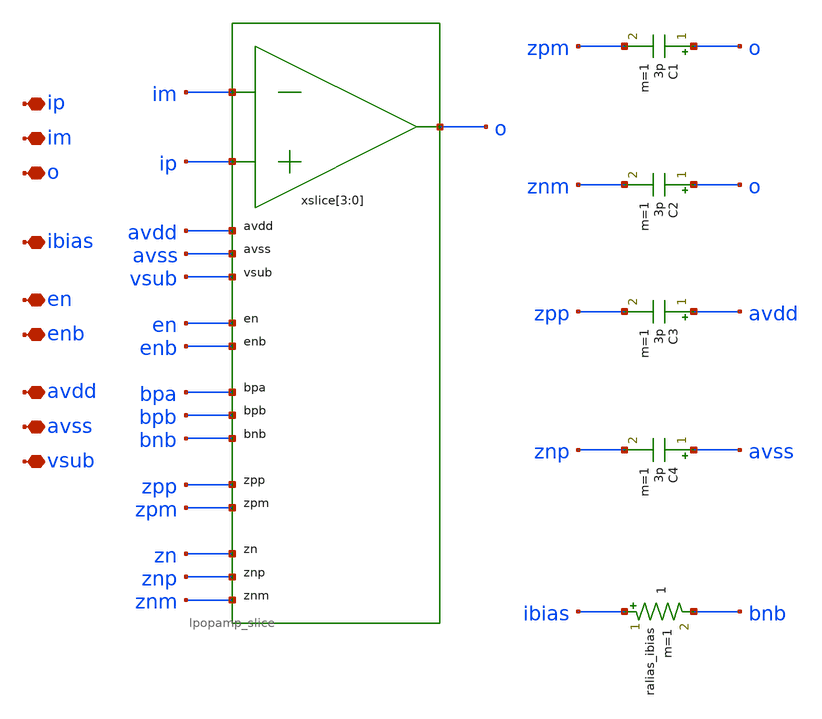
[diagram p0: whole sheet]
** sch_path: xschem/lpopamp_ref.sch
**.subckt lpopamp_ref avdd avss ip im o ibias en enb vsub
*.iopin avdd
*.iopin avss
*.iopin ip
*.iopin im
*.iopin o
*.iopin ibias
*.iopin en
*.iopin enb
*.iopin vsub
xslice[3] im ip o avdd avss en enb bpa bpb bnb zpp zpm zn znp znm lpopamp_slice
xslice[2] im ip o avdd avss en enb bpa bpb bnb zpp zpm zn znp znm lpopamp_slice
xslice[1] im ip o avdd avss en enb bpa bpb bnb zpp zpm zn znp znm lpopamp_slice
xslice[0] im ip o avdd avss en enb bpa bpb bnb zpp zpm zn znp znm lpopamp_slice
ralias_ibias ibias bnb 1 m=1
C1 o zpm 3p m=1
C2 o znm 3p m=1
C3 avdd zpp 3p m=1
C4 avss znp 3p m=1
**.ends
.end
